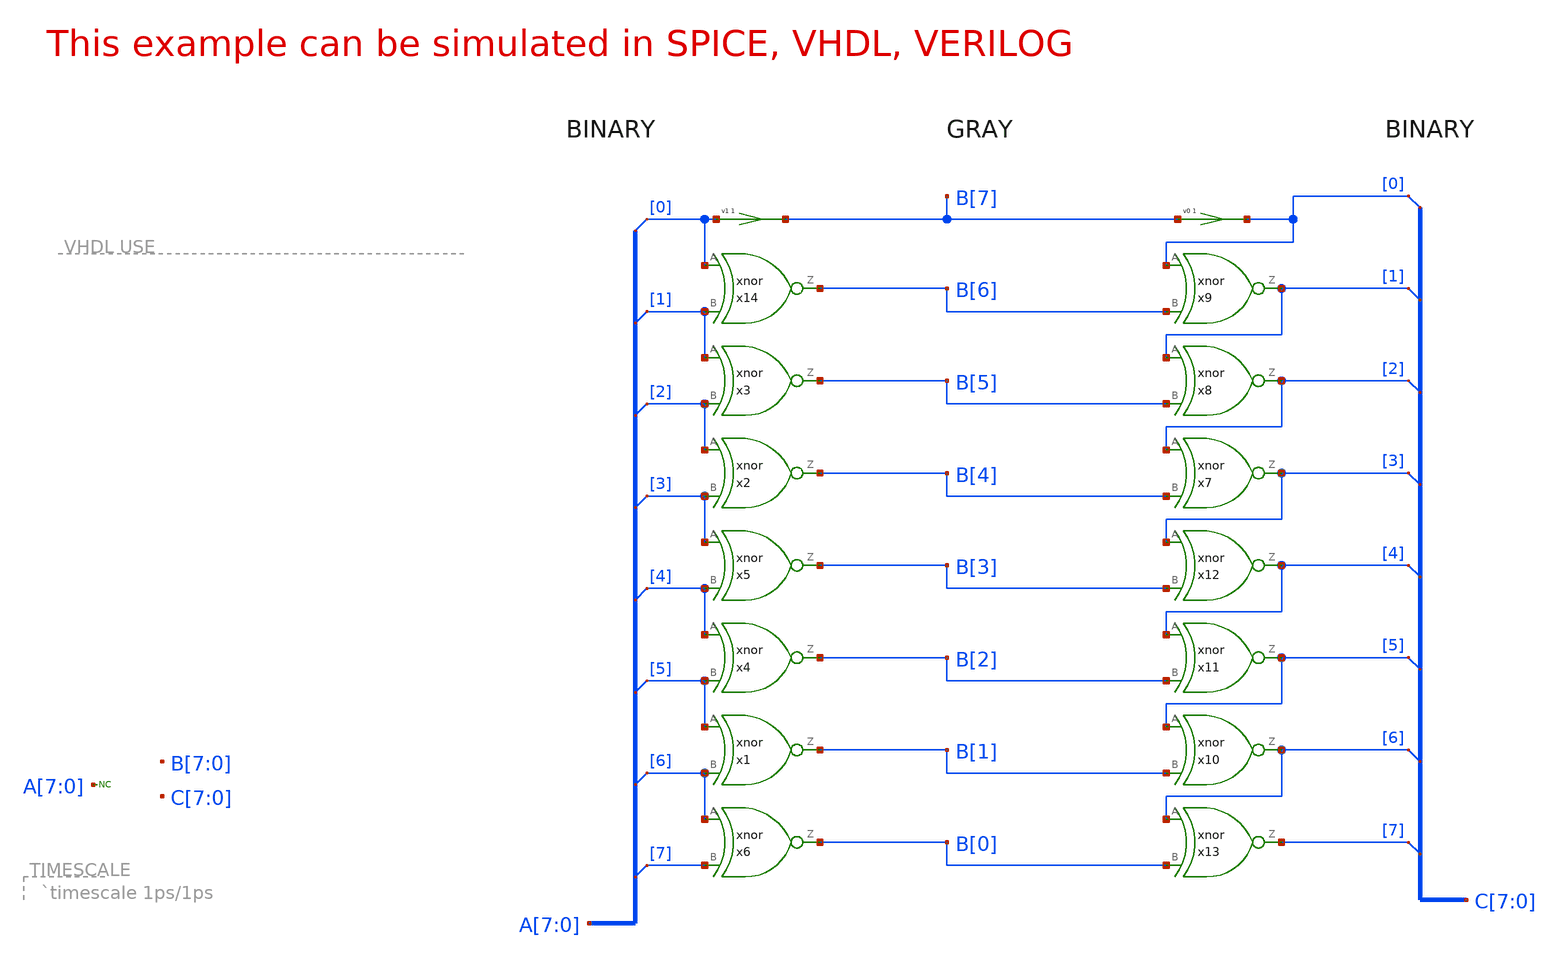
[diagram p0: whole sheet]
** sch_path: examples/xschem_examples/greycnt.sch
* Copyright (C) 1998-2023 Stefan Frederik Schippers
* This program is free software; you can redistribute it and/or modify
* it under the terms of the GNU General Public License as published by
* the Free Software Foundation; either version 2 of the License, or
* (at your option) any later version.
* This program is distributed in the hope that it will be useful,
* but WITHOUT ANY WARRANTY; without even the implied warranty of
* MERCHANTABILITY or FITNESS FOR A PARTICULAR PURPOSE.  See the
* GNU General Public License for more details.
* You should have received a copy of the GNU General Public License
* along with this program; if not, write to the Free Software
**.subckt greycnt
x2 B[4] A[2] A[3] xnor
x3 B[5] A[1] A[2] xnor
x14 B[6] A[0] A[1] xnor
v1 B[7] A[0] 0
x1 B[1] A[5] A[6] xnor
x4 B[2] A[4] A[5] xnor
x5 B[3] A[3] A[4] xnor
x6 B[0] A[6] A[7] xnor
x7 C[3] C[2] B[4] xnor
x8 C[2] C[1] B[5] xnor
x9 C[1] C[0] B[6] xnor
v0 C[0] B[7] 0
x10 C[6] C[5] B[1] xnor
x11 C[5] C[4] B[2] xnor
x12 C[4] C[3] B[3] xnor
x13 C[7] C[6] B[0] xnor
* noconn A[7:0]
* tap: C[7:0] --> C[0]
* tap: C[7:0] --> C[1]
* tap: C[7:0] --> C[2]
* tap: C[7:0] --> C[3]
* tap: C[7:0] --> C[4]
* tap: C[7:0] --> C[5]
* tap: C[7:0] --> C[6]
* tap: C[7:0] --> C[7]
* tap: A[7:0] --> A[0]
* tap: A[7:0] --> A[1]
* tap: A[7:0] --> A[2]
* tap: A[7:0] --> A[3]
* tap: A[7:0] --> A[4]
* tap: A[7:0] --> A[5]
* tap: A[7:0] --> A[6]
* tap: A[7:0] --> A[7]
**** begin user architecture code

.tran 1n 2000n

* to generate following file copy .../share/doc/xschem/examples/stimuli.greycnt
* to the simulation directory and run simulation -> Utile Stimuli Editor (GUI),
* and press 'Translate'
.include stimuli_greycnt.cir

.model nmos NMOS  LEVEL=1  LMIN=0.5e-6 LMAX=50e-6 WMIN=0.9e-6 WMAX=1  VTO=0.7 GAMMA=0.45 PHI=0.9
+  NSUB=9e14 LD=0.08e-6 UO=350 LAMBDA=0.1  TOX=9e-9 PB=0.9 CJ=0.56e-3 CJSW=0.35e-11  MJ=0.45 MJSW=0.2
+ CGDO=0.4e-9 JS=1.0e-8
.model pmos PMOS  LEVEL=1  LMIN=0.5e-6 LMAX=50e-6 WMIN=0.9e-6 WMAX=1  VTO=-0.8 GAMMA=0.4 PHI=0.8
+  NSUB=5e14 LD=0.09e-6 UO=100 LAMBDA=0.2  TOX=9e-9 PB=0.9 CJ=0.94e-3 CJSW=0.32e-11  MJ=0.5 MJSW=0.3 CGDO=0.3e-9
+ JS=0.5e-8
**** end user architecture code
**.ends

* expanding   symbol:  xnor.sym # of pins=3
** sym_path: examples/xschem_examples/xnor.sym
** sch_path: examples/xschem_examples/xnor.sch
.subckt xnor Z A B  risedel=400 falldel=300
*.ipin B
*.opin Z
*.ipin A
M1 net2 A GND GND nmos w=10u l=1u m=1
M2 net3 net1 GND GND nmos w=10u l=1u m=1
M3 Z A net3 GND nmos w=10u l=1u m=1
M4 Z B net3 GND nmos w=10u l=1u m=1
M5 net1 B net2 GND nmos w=10u l=1u m=1
M6 net1 A VDD VDD pmos w=10u l=1u m=1
M7 net1 B VDD VDD pmos w=10u l=1u m=1
M8 net4 A VDD VDD pmos w=10u l=1u m=1
M9 Z B net4 VDD pmos w=10u l=1u m=1
M10 Z net1 VDD VDD pmos w=10u l=1u m=1
.ends

.GLOBAL GND
.GLOBAL VDD
.end
